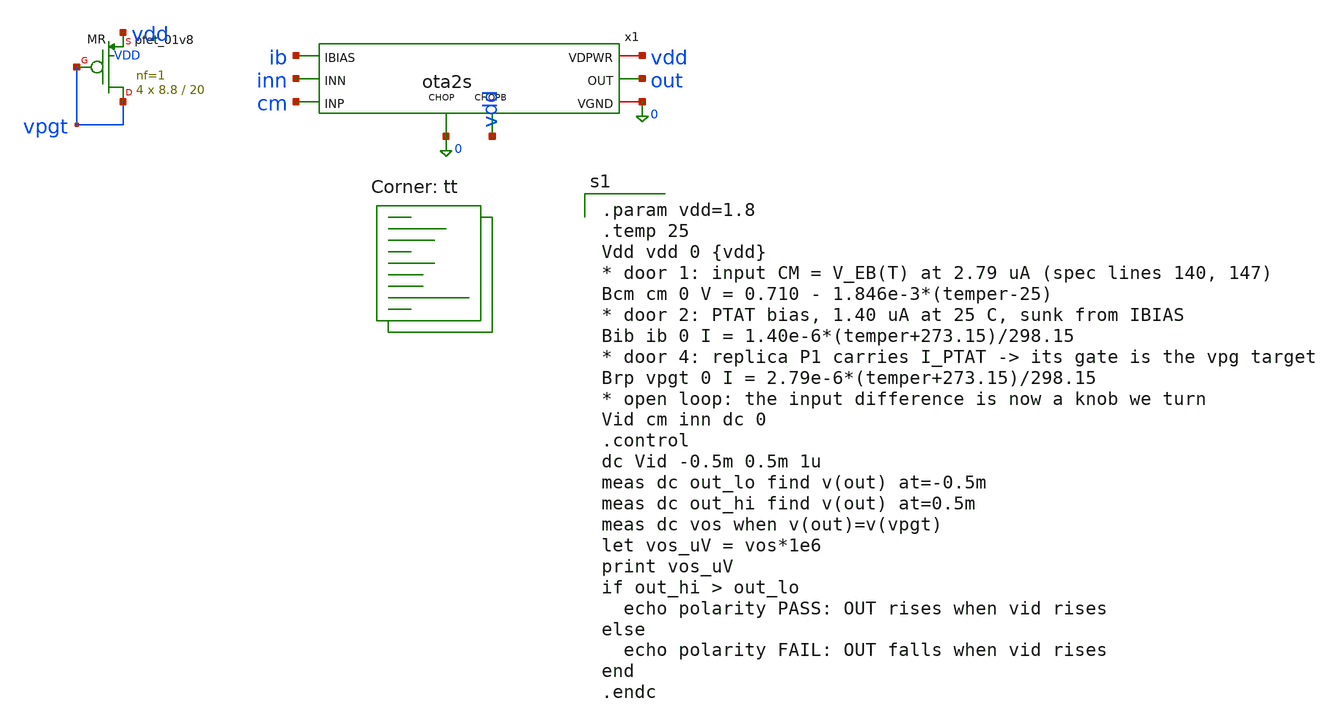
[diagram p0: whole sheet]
** sch_path: xschem/tb_ota2s_pol.sch
**.subckt tb_ota2s_pol
x1 cm inn out vdd 0 ib 0 vdd ota2s
XMR vpgt vpgt vdd VDD sky130_fd_pr__pfet_01v8 L=20 W=8.8 nf=1 ad='int((1 + 1)/2) * 8.8 / 1 * 0.29' as='int((1 + 2)/2) * 8.8 / 1 * 0.29'
+ pd='2*int((1 + 1)/2) * (8.8 / 1 + 0.29)' ps='2*int((1 + 2)/2) * (8.8 / 1 + 0.29)' nrd='0.29 / 8.8 ' nrs='0.29 / 8.8 '
+ sa=0 sb=0 sd=0 mult=4 m=4
**** begin user architecture code
.lib $::SKYWATER_MODELS/sky130.lib.spice tt

.param vdd=1.8
.temp 25
Vdd vdd 0 {vdd}
* door 1: input CM = V_EB(T) at 2.79 uA (spec lines 140, 147)
Bcm cm 0 V = 0.710 - 1.846e-3*(temper-25)
* door 2: PTAT bias, 1.40 uA at 25 C, sunk from IBIAS
Bib ib 0 I = 1.40e-6*(temper+273.15)/298.15
* door 4: replica P1 carries I_PTAT -> its gate is the vpg target
Brp vpgt 0 I = 2.79e-6*(temper+273.15)/298.15
* open loop: the input difference is now a knob we turn
Vid cm inn dc 0
.control
dc Vid -0.5m 0.5m 1u
meas dc out_lo find v(out) at=-0.5m
meas dc out_hi find v(out) at=0.5m
meas dc vos when v(out)=v(vpgt)
let vos_uV = vos*1e6
print vos_uV
if out_hi > out_lo
  echo polarity PASS: OUT rises when vid rises
else
  echo polarity FAIL: OUT falls when vid rises
end
.endc

**** end user architecture code
**.ends

* expanding   symbol:  ota2s.sym # of pins=8
** sym_path: xschem/ota2s.sym
** sch_path: xschem/ota2s.sch
.subckt ota2s INP INN OUT VDPWR VGND IBIAS CHOP CHOPB
*.ipin INN
*.ipin INP
*.ipin IBIAS
*.opin OUT
*.iopin VDPWR
*.iopin VGND
*.ipin CHOPB
*.ipin CHOP
XMREF IBIAS IBIAS VDPWR VDPWR sky130_fd_pr__pfet_01v8 L=4 W=20 nf=1 ad='int((1 + 1)/2) * 20 / 1 * 0.29'
+ as='int((1 + 2)/2) * 20 / 1 * 0.29' pd='2*int((1 + 1)/2) * (20 / 1 + 0.29)' ps='2*int((1 + 2)/2) * (20 / 1 + 0.29)'
+ nrd='0.29 / 20 ' nrs='0.29 / 20 ' sa=0 sb=0 sd=0 mult=1 m=1
XMTAIL tail IBIAS VDPWR VDPWR sky130_fd_pr__pfet_01v8 L=4 W=20 nf=1 ad='int((1 + 1)/2) * 20 / 1 * 0.29'
+ as='int((1 + 2)/2) * 20 / 1 * 0.29' pd='2*int((1 + 1)/2) * (20 / 1 + 0.29)' ps='2*int((1 + 2)/2) * (20 / 1 + 0.29)'
+ nrd='0.29 / 20 ' nrs='0.29 / 20 ' sa=0 sb=0 sd=0 mult=2 m=2
XMP1 d1 INN tail VDPWR sky130_fd_pr__pfet_01v8_lvt L=6 W=25 nf=1 ad='int((1 + 1)/2) * 25 / 1 * 0.29'
+ as='int((1 + 2)/2) * 25 / 1 * 0.29' pd='2*int((1 + 1)/2) * (25 / 1 + 0.29)' ps='2*int((1 + 2)/2) * (25 / 1 + 0.29)'
+ nrd='0.29 / 25 ' nrs='0.29 / 25 ' sa=0 sb=0 sd=0 mult=24 m=24
XMP2 x1 INP tail VDPWR sky130_fd_pr__pfet_01v8_lvt L=6 W=25 nf=1 ad='int((1 + 1)/2) * 25 / 1 * 0.29'
+ as='int((1 + 2)/2) * 25 / 1 * 0.29' pd='2*int((1 + 1)/2) * (25 / 1 + 0.29)' ps='2*int((1 + 2)/2) * (25 / 1 + 0.29)'
+ nrd='0.29 / 25 ' nrs='0.29 / 25 ' sa=0 sb=0 sd=0 mult=24 m=24
XMN1 d1 g12 VGND VGND sky130_fd_pr__nfet_01v8 L=20 W=6 nf=1 ad='int((1 + 1)/2) * 6 / 1 * 0.29' as='int((1 + 2)/2) * 6 / 1 * 0.29'
+ pd='2*int((1 + 1)/2) * (6 / 1 + 0.29)' ps='2*int((1 + 2)/2) * (6 / 1 + 0.29)' nrd='0.29 / 6 ' nrs='0.29 / 6 '
+ sa=0 sb=0 sd=0 mult=2 m=2
XMN2 x1 g12 VGND VGND sky130_fd_pr__nfet_01v8 L=20 W=6 nf=1 ad='int((1 + 1)/2) * 6 / 1 * 0.29' as='int((1 + 2)/2) * 6 / 1 * 0.29'
+ pd='2*int((1 + 1)/2) * (6 / 1 + 0.29)' ps='2*int((1 + 2)/2) * (6 / 1 + 0.29)' nrd='0.29 / 6 ' nrs='0.29 / 6 '
+ sa=0 sb=0 sd=0 mult=2 m=2
XMP3 OUT IBIAS VDPWR VDPWR sky130_fd_pr__pfet_01v8 L=4 W=20 nf=1 ad='int((1 + 1)/2) * 20 / 1 * 0.29'
+ as='int((1 + 2)/2) * 20 / 1 * 0.29' pd='2*int((1 + 1)/2) * (20 / 1 + 0.29)' ps='2*int((1 + 2)/2) * (20 / 1 + 0.29)'
+ nrd='0.29 / 20 ' nrs='0.29 / 20 ' sa=0 sb=0 sd=0 mult=6 m=6
XMN3 OUT g3 VGND VGND sky130_fd_pr__nfet_01v8 L=1 W=7 nf=1 ad='int((1 + 1)/2) * 7 / 1 * 0.29' as='int((1 + 2)/2) * 7 / 1 * 0.29'
+ pd='2*int((1 + 1)/2) * (7 / 1 + 0.29)' ps='2*int((1 + 2)/2) * (7 / 1 + 0.29)' nrd='0.29 / 7 ' nrs='0.29 / 7 '
+ sa=0 sb=0 sd=0 mult=1 m=1
XRZ1 net1 g3 VGND sky130_fd_pr__res_high_po_1p41 L=20 mult=1 m=1
XRZ2 net2 net1 VGND sky130_fd_pr__res_high_po_1p41 L=20 mult=1 m=1
XRZ3 net3 net2 VGND sky130_fd_pr__res_high_po_1p41 L=20 mult=1 m=1
XRZ4 net4 net3 VGND sky130_fd_pr__res_high_po_1p41 L=20 mult=1 m=1
XRZ5 net5 net4 VGND sky130_fd_pr__res_high_po_1p41 L=20 mult=1 m=1
XRZ6 cz net5 VGND sky130_fd_pr__res_high_po_1p41 L=20 mult=1 m=1
XCC cz OUT sky130_fd_pr__cap_mim_m3_1 W=25 L=25 MF=8 m=8
XDP tail VDPWR tail VDPWR sky130_fd_pr__pfet_01v8_lvt L=6 W=25 nf=1 ad='int((1 + 1)/2) * 25 / 1 * 0.29'
+ as='int((1 + 2)/2) * 25 / 1 * 0.29' pd='2*int((1 + 1)/2) * (25 / 1 + 0.29)' ps='2*int((1 + 2)/2) * (25 / 1 + 0.29)'
+ nrd='0.29 / 25 ' nrs='0.29 / 25 ' sa=0 sb=0 sd=0 mult=8 m=8
XDNA d1 VGND VGND VGND sky130_fd_pr__nfet_01v8 L=20 W=6 nf=1 ad='int((1 + 1)/2) * 6 / 1 * 0.29' as='int((1 + 2)/2) * 6 / 1 * 0.29'
+ pd='2*int((1 + 1)/2) * (6 / 1 + 0.29)' ps='2*int((1 + 2)/2) * (6 / 1 + 0.29)' nrd='0.29 / 6 ' nrs='0.29 / 6 '
+ sa=0 sb=0 sd=0 mult=2 m=2
XDNB x1 VGND VGND VGND sky130_fd_pr__nfet_01v8 L=20 W=6 nf=1 ad='int((1 + 1)/2) * 6 / 1 * 0.29' as='int((1 + 2)/2) * 6 / 1 * 0.29'
+ pd='2*int((1 + 1)/2) * (6 / 1 + 0.29)' ps='2*int((1 + 2)/2) * (6 / 1 + 0.29)' nrd='0.29 / 6 ' nrs='0.29 / 6 '
+ sa=0 sb=0 sd=0 mult=2 m=2
XDB VDPWR VDPWR VDPWR VDPWR sky130_fd_pr__pfet_01v8 L=4 W=20 nf=1 ad='int((1 + 1)/2) * 20 / 1 * 0.29'
+ as='int((1 + 2)/2) * 20 / 1 * 0.29' pd='2*int((1 + 1)/2) * (20 / 1 + 0.29)' ps='2*int((1 + 2)/2) * (20 / 1 + 0.29)'
+ nrd='0.29 / 20 ' nrs='0.29 / 20 ' sa=0 sb=0 sd=0 mult=2 m=2
XRD1 VGND VGND VGND sky130_fd_pr__res_high_po_1p41 L=20 mult=1 m=1
XRD2 VGND VGND VGND sky130_fd_pr__res_high_po_1p41 L=20 mult=1 m=1
XSD1 d1 CHOPB g12 VGND sky130_fd_pr__nfet_01v8 L=0.5 W=6 nf=1 ad='int((1 + 1)/2) * 6 / 1 * 0.29' as='int((1 + 2)/2) * 6 / 1 * 0.29'
+ pd='2*int((1 + 1)/2) * (6 / 1 + 0.29)' ps='2*int((1 + 2)/2) * (6 / 1 + 0.29)' nrd='0.29 / 6 ' nrs='0.29 / 6 '
+ sa=0 sb=0 sd=0 mult=1 m=1
XSD2 x1 CHOP g12 VGND sky130_fd_pr__nfet_01v8 L=0.5 W=6 nf=1 ad='int((1 + 1)/2) * 6 / 1 * 0.29' as='int((1 + 2)/2) * 6 / 1 * 0.29'
+ pd='2*int((1 + 1)/2) * (6 / 1 + 0.29)' ps='2*int((1 + 2)/2) * (6 / 1 + 0.29)' nrd='0.29 / 6 ' nrs='0.29 / 6 '
+ sa=0 sb=0 sd=0 mult=1 m=1
XSG2 g3 CHOP d1 VGND sky130_fd_pr__nfet_01v8 L=0.5 W=6 nf=1 ad='int((1 + 1)/2) * 6 / 1 * 0.29' as='int((1 + 2)/2) * 6 / 1 * 0.29'
+ pd='2*int((1 + 1)/2) * (6 / 1 + 0.29)' ps='2*int((1 + 2)/2) * (6 / 1 + 0.29)' nrd='0.29 / 6 ' nrs='0.29 / 6 '
+ sa=0 sb=0 sd=0 mult=1 m=1
XSG1 x1 CHOPB g3 VGND sky130_fd_pr__nfet_01v8 L=0.5 W=6 nf=1 ad='int((1 + 1)/2) * 6 / 1 * 0.29' as='int((1 + 2)/2) * 6 / 1 * 0.29'
+ pd='2*int((1 + 1)/2) * (6 / 1 + 0.29)' ps='2*int((1 + 2)/2) * (6 / 1 + 0.29)' nrd='0.29 / 6 ' nrs='0.29 / 6 '
+ sa=0 sb=0 sd=0 mult=1 m=1
.ends

.end
